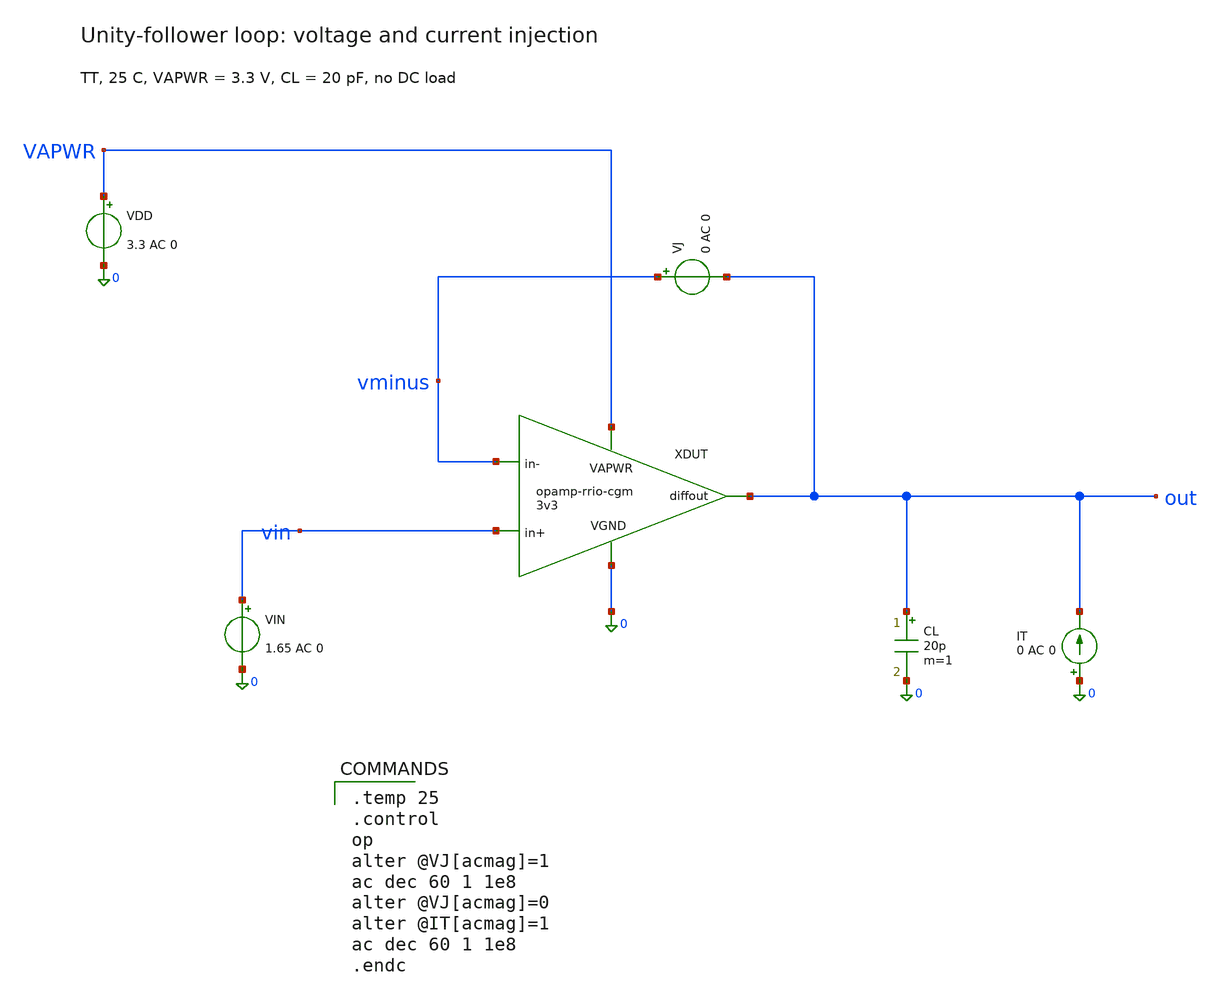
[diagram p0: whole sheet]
** sch_path: docs/simulation/xschem/bench-loop.sch
**.subckt bench-loop
XDUT VAPWR out vin vminus 0 opamp-rrio-cgm-3v3
VDD VAPWR 0 3.3 AC 0
VIN vin 0 1.65 AC 0
CL out 0 20p m=1
VJ vminus out 0 AC 0
IT 0 out 0 AC 0
**** begin user architecture code
 .lib $::SKYWATER_MODELS/sky130.lib.spice tt

.temp 25
.control
op
alter @VJ[acmag]=1
ac dec 60 1 1e8
alter @VJ[acmag]=0
alter @IT[acmag]=1
ac dec 60 1 1e8
.endc

**** end user architecture code
**.ends
.end
